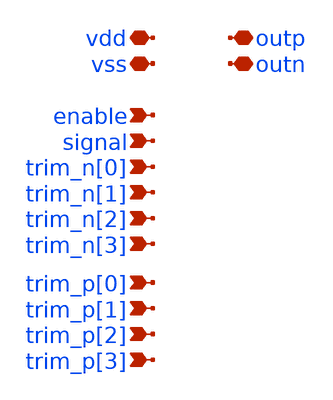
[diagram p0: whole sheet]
** sch_path: xschem/untitled.sch
**.subckt untitled enable signal trim_n[0] trim_n[1] trim_n[2] trim_n[3] trim_p[0] trim_p[1]
*+ trim_p[2] trim_p[3] vss vdd outp outn
*.ipin enable
*.ipin signal
*.ipin trim_n[0]
*.ipin trim_n[1]
*.ipin trim_n[2]
*.ipin trim_n[3]
*.ipin trim_p[0]
*.ipin trim_p[1]
*.ipin trim_p[2]
*.ipin trim_p[3]
*.iopin vss
*.iopin vdd
*.iopin outp
*.iopin outn
**** begin user architecture code


.subckt injector_flat enable outn outp signal trim_n[0] trim_n[1] trim_n[2] trim_n[3]  trim_p[0]
+ trim_p[1] trim_p[2] trim_p[3] vss vdd
X0 vdd a_9644_7080# a_9556_7124# vdd pmos_6p0 w=1.22u l=1u
X1 outn _00_ vss vss nmos_6p0 w=0.82u l=0.6u
X2 vdd _21_ a_2500_4539# vdd pmos_6p0 w=0.62u l=0.5u
X3 _13_ a_8412_4728# vss vss nmos_6p0 w=0.82u l=0.6u
X4 outn _00_ vdd vdd pmos_6p0 w=1.22u l=0.5u
X5 a_2588_5512# a_2500_5556# vss vss nmos_6p0 w=0.82u l=1u
X6 vdd a_3036_5079# a_2948_5176# vdd pmos_6p0 w=1.22u l=1u
X7 a_3044_3229# a_2612_3229# vss vss nmos_6p0 w=0.36u l=0.6u
X8 outp _00_ vdd vdd pmos_6p0 w=1.22u l=0.5u
X9 vdd _08_ outp vdd pmos_6p0 w=1.22u l=0.5u
X10 outn _01_ vdd vdd pmos_6p0 w=1.22u l=0.5u
X11 outn _01_ vss vss nmos_6p0 w=0.82u l=0.6u
X12 outn _00_ vss vss nmos_6p0 w=0.82u l=0.6u
X13 vdd _00_ outp vdd pmos_6p0 w=1.22u l=0.5u
X14 vss a_17700_7124# _07_ vss nmos_6p0 w=0.82u l=0.6u
X15 vdd _24_ a_7092_3229# vdd pmos_6p0 w=0.62u l=0.5u
X16 vss trim_p[1] a_7204_7933# vss nmos_6p0 w=0.36u l=0.6u
X17 outp _00_ vdd vdd pmos_6p0 w=1.22u l=0.5u
X18 outn _00_ vdd vdd pmos_6p0 w=1.22u l=0.5u
X19 _00_ enable vdd vdd pmos_6p0 w=1.22u l=0.5u
X20 outn _00_ vdd vdd pmos_6p0 w=1.22u l=0.5u
X21 outp _00_ vdd vdd pmos_6p0 w=1.22u l=0.5u
X22 a_8573_7889# _00_ vss vss nmos_6p0 w=0.36u l=0.6u
X23 vdd _14_ outp vdd pmos_6p0 w=1.22u l=0.5u
X24 outp _00_ vdd vdd pmos_6p0 w=1.22u l=0.5u
X25 a_16812_3944# a_16724_3988# vss vss nmos_6p0 w=0.82u l=1u
X26 outp _00_ vss vss nmos_6p0 w=0.82u l=0.6u
X27 vdd _00_ outn vdd pmos_6p0 w=1.22u l=0.5u
X28 vdd a_16924_7080# a_16836_7124# vdd pmos_6p0 w=1.22u l=1u
X29 a_15171_7933# a_14708_7933# vss vss nmos_6p0 w=0.36u l=0.6u
X30 vdd a_3484_5079# a_3396_5176# vdd pmos_6p0 w=1.22u l=1u
X31 outn _00_ vdd vdd pmos_6p0 w=1.22u l=0.5u
X32 outp _00_ vss vss nmos_6p0 w=0.82u l=0.6u
X33 vdd _17_ outn vdd pmos_6p0 w=1.22u l=0.5u
X34 a_16280_3604# trim_n[3] vss vss nmos_6p0 w=0.36u l=0.6u
X35 outp _00_ vdd vdd pmos_6p0 w=1.22u l=0.5u
X36 a_12575_3988# a_12132_4539# vdd vdd pmos_6p0 w=0.62u l=0.5u
X37 vdd _26_ a_11124_3229# vdd pmos_6p0 w=0.62u l=0.5u
X38 a_3044_3229# a_2612_3229# a_3004_3696# vdd pmos_6p0 w=0.62u l=0.5u
X39 a_5724_5512# a_5636_5556# vss vss nmos_6p0 w=0.82u l=1u
X40 a_3981_7889# _00_ vss vss nmos_6p0 w=0.36u l=0.6u
X41 outp _00_ vss vss nmos_6p0 w=0.82u l=0.6u
X42 outp _00_ vdd vdd pmos_6p0 w=1.22u l=0.5u
X43 outn _00_ vss vss nmos_6p0 w=0.82u l=0.6u
X44 a_2588_6647# a_2500_6744# vss vss nmos_6p0 w=0.82u l=1u
X45 a_12892_5079# a_12804_5176# vss vss nmos_6p0 w=0.82u l=1u
X46 a_15375_7124# a_14932_7675# vdd vdd pmos_6p0 w=0.62u l=0.5u
X47 _26_ a_5836_3160# vss vss nmos_6p0 w=0.82u l=0.6u
X48 a_16280_3604# trim_n[3] vdd vdd pmos_6p0 w=0.62u l=0.5u
X49 a_1692_5512# a_1604_5556# vss vss nmos_6p0 w=0.82u l=1u
X50 _21_ a_2028_3160# vss vss nmos_6p0 w=0.82u l=0.6u
X51 outn a_7555_4539# vss vss nmos_6p0 w=0.82u l=0.6u
X52 vss _11_ outn vss nmos_6p0 w=0.82u l=0.6u
X53 vdd a_2140_5079# a_2052_5176# vdd pmos_6p0 w=1.22u l=1u
X54 outn _13_ vdd vdd pmos_6p0 w=1.22u l=0.5u
X55 vss a_8328_3604# a_7555_3229# vss nmos_6p0 w=0.36u l=0.6u
X56 a_16851_4797# a_16388_4797# vss vss nmos_6p0 w=0.36u l=0.6u
X57 outp _00_ vdd vdd pmos_6p0 w=1.22u l=0.5u
X58 a_7524_7675# a_7092_7156# vss vss nmos_6p0 w=0.36u l=0.6u
X59 vss a_3044_7675# outp vss nmos_6p0 w=0.82u l=0.6u
X60 a_15487_3728# a_16280_3604# a_15507_3229# vdd pmos_6p0 w=0.62u l=0.5u
X61 vss a_17028_6744# _08_ vss nmos_6p0 w=0.82u l=0.6u
X62 a_12595_4539# a_12132_4539# vss vss nmos_6p0 w=0.36u l=0.6u
X63 _25_ a_6508_3160# vss vss nmos_6p0 w=0.82u l=0.6u
X64 a_6508_6647# a_6420_6744# vss vss nmos_6p0 w=0.82u l=1u
X65 outp _00_ vss vss nmos_6p0 w=0.82u l=0.6u
X66 vss trim_n[0] a_2612_3229# vss nmos_6p0 w=0.36u l=0.6u
X67 vss a_3044_3229# outp vss nmos_6p0 w=0.82u l=0.6u
X68 outn a_2963_4539# vss vss nmos_6p0 w=0.82u l=0.6u
X69 outp a_15151_8432# vdd vdd pmos_6p0 w=1.095u l=0.5u
X70 _02_ a_5636_8000# vss vss nmos_6p0 w=0.82u l=0.6u
X71 vdd a_16700_8215# a_16612_8312# vdd pmos_6p0 w=1.22u l=1u
X72 a_12360_8308# trim_p[2] vss vss nmos_6p0 w=0.36u l=0.6u
X73 a_3036_5512# a_2948_5556# vss vss nmos_6p0 w=0.82u l=1u
X74 _03_ a_4771_7124# vdd vdd pmos_6p0 w=1.22u l=0.5u
X75 vdd a_17932_8215# a_17844_8312# vdd pmos_6p0 w=1.22u l=1u
X76 vdd a_4828_5512# a_4740_5556# vdd pmos_6p0 w=1.22u l=1u
X77 a_3505_6296# _00_ vss vss nmos_6p0 w=0.36u l=0.6u
X78 vdd a_8573_7889# a_7596_8400# vdd pmos_6p0 w=0.62u l=0.5u
X79 vdd a_4492_3944# a_4404_3988# vdd pmos_6p0 w=1.22u l=1u
X80 a_2943_3988# a_3736_3976# a_2963_4539# vdd pmos_6p0 w=0.62u l=0.5u
X81 vss a_3505_6296# _04_ vss nmos_6p0 w=0.82u l=0.6u
X82 vdd a_8461_7553# a_7484_7156# vdd pmos_6p0 w=0.62u l=0.5u
X83 a_4828_4728# a_4828_4728# vdd vdd pmos_6p0 w=1.22u l=0.5u
X84 a_1692_6647# a_1604_6744# vss vss nmos_6p0 w=0.82u l=1u
X85 vss trim_p[2] a_12020_7156# vss nmos_6p0 w=0.36u l=0.6u
X86 vss a_16280_3604# a_15507_3229# vss nmos_6p0 w=0.36u l=0.6u
X87 vss a_3044_7933# outn vss nmos_6p0 w=0.82u l=0.6u
X88 outp _00_ vss vss nmos_6p0 w=0.82u l=0.6u
X89 a_3484_5512# a_3396_5556# vss vss nmos_6p0 w=0.82u l=1u
X90 _01_ a_1716_8000# vss vss nmos_6p0 w=0.82u l=0.6u
X91 vdd a_9644_3944# a_9556_3988# vdd pmos_6p0 w=1.22u l=1u
X92 a_5612_6647# a_5524_6744# vss vss nmos_6p0 w=0.82u l=1u
X93 vdd a_14012_8215# a_13924_8312# vdd pmos_6p0 w=1.22u l=1u
X94 outp _00_ vss vss nmos_6p0 w=0.82u l=0.6u
X95 vdd trim_n[1] a_7535_3988# vdd pmos_6p0 w=0.62u l=0.5u
X96 a_12412_7156# trim_p[2] a_12452_7675# vss nmos_6p0 w=0.36u l=0.6u
X97 vdd _03_ a_5636_8000# vdd pmos_6p0 w=0.565u l=0.5u
X98 a_3036_6647# a_2948_6744# vss vss nmos_6p0 w=0.82u l=1u
X99 a_7555_3229# a_7092_3229# vss vss nmos_6p0 w=0.36u l=0.6u
X100 a_3981_7553# _00_ vdd vdd pmos_6p0 w=0.62u l=0.5u
X101 a_16831_5296# a_17624_5172# a_16851_4797# vdd pmos_6p0 w=0.62u l=0.5u
X102 vdd a_17700_5556# a_17700_5556# vdd pmos_6p0 w=1.22u l=0.5u
X103 vss _03_ a_5636_8000# vss nmos_6p0 w=0.36u l=0.6u
X104 a_2140_5512# a_2052_5556# vss vss nmos_6p0 w=0.82u l=1u
X105 vdd a_3932_5512# a_3844_5556# vdd pmos_6p0 w=1.22u l=1u
X106 a_4771_7124# _00_ vss vss nmos_6p0 w=0.36u l=0.6u
X107 a_3044_7933# a_2612_7933# a_3004_8400# vdd pmos_6p0 w=0.62u l=0.5u
X108 vdd a_2588_6647# a_2500_6744# vdd pmos_6p0 w=1.22u l=1u
X109 a_8573_7889# _00_ vdd vdd pmos_6p0 w=0.62u l=0.5u
X110 a_8461_7553# _00_ vdd vdd pmos_6p0 w=0.62u l=0.5u
X111 a_3004_3696# trim_n[0] vdd vdd pmos_6p0 w=0.62u l=0.5u
X112 vss _15_ outn vss nmos_6p0 w=0.82u l=0.6u
X113 vss a_12360_8308# a_11587_7933# vss nmos_6p0 w=0.36u l=0.6u
X114 a_3004_3696# trim_n[0] a_3044_3229# vss nmos_6p0 w=0.36u l=0.6u
X115 a_15151_8432# a_14708_7933# vdd vdd pmos_6p0 w=0.62u l=0.5u
X116 vss a_3981_7889# a_3044_7933# vss nmos_6p0 w=0.36u l=0.6u
X117 _20_ a_16364_4428# vss vss nmos_6p0 w=0.82u l=0.6u
X118 outn a_12595_4539# vss vss nmos_6p0 w=0.82u l=0.6u
X119 a_11587_3229# a_11124_3229# vss vss nmos_6p0 w=0.36u l=0.6u
X120 vdd a_2588_5512# a_2500_5556# vdd pmos_6p0 w=1.22u l=1u
X121 vdd a_17028_6744# a_17028_6744# vdd pmos_6p0 w=1.22u l=0.5u
X122 a_5836_4428# a_5836_4428# vdd vdd pmos_6p0 w=1.22u l=0.5u
X123 vdd a_6508_6647# a_6420_6744# vdd pmos_6p0 w=1.22u l=1u
X124 a_3981_7889# _00_ vdd vdd pmos_6p0 w=0.62u l=0.5u
X125 outn _09_ vdd vdd pmos_6p0 w=1.22u l=0.5u
X126 outp _02_ vdd vdd pmos_6p0 w=1.22u l=0.5u
X127 a_15507_3229# trim_n[3] a_15487_3728# vss nmos_6p0 w=0.36u l=0.6u
X128 a_5276_5512# a_5188_5556# vss vss nmos_6p0 w=0.82u l=1u
X129 vss a_3736_3976# a_2963_4539# vss nmos_6p0 w=0.36u l=0.6u
X130 vdd a_7484_7156# outp vdd pmos_6p0 w=1.095u l=0.5u
X131 vdd trim_n[1] a_7535_3728# vdd pmos_6p0 w=0.62u l=0.5u
X132 vdd trim_p[3] a_15375_7124# vdd pmos_6p0 w=0.62u l=0.5u
X133 a_16364_6296# a_16364_6296# vdd vdd pmos_6p0 w=1.22u l=0.5u
X134 vdd a_7596_8400# outn vdd pmos_6p0 w=1.095u l=0.5u
X135 outn _00_ vdd vdd pmos_6p0 w=1.22u l=0.5u
X136 outn _00_ vss vss nmos_6p0 w=0.82u l=0.6u
X137 vdd a_12892_5079# a_12804_5176# vdd pmos_6p0 w=1.22u l=1u
X138 vdd a_16812_3944# a_16724_3988# vdd pmos_6p0 w=1.22u l=1u
X139 vdd _11_ outn vdd pmos_6p0 w=1.22u l=0.5u
X140 a_16831_5296# a_16388_4797# vdd vdd pmos_6p0 w=0.62u l=0.5u
X141 outn _00_ vss vss nmos_6p0 w=0.82u l=0.6u
X142 a_2140_6647# a_2052_6744# vss vss nmos_6p0 w=0.82u l=1u
X143 outn _00_ vdd vdd pmos_6p0 w=1.22u l=0.5u
X144 outp _00_ vdd vdd pmos_6p0 w=1.22u l=0.5u
X145 outp _00_ vss vss nmos_6p0 w=0.82u l=0.6u
X146 vdd _00_ a_14708_7933# vdd pmos_6p0 w=0.62u l=0.5u
X147 a_12452_7675# a_12020_7156# vss vss nmos_6p0 w=0.36u l=0.6u
X148 vdd trim_n[2] a_11567_3728# vdd pmos_6p0 w=0.62u l=0.5u
X149 vdd a_5724_5512# a_5636_5556# vdd pmos_6p0 w=1.22u l=1u
X150 vdd a_1692_6647# a_1604_6744# vdd pmos_6p0 w=1.22u l=1u
X151 outn _00_ vdd vdd pmos_6p0 w=1.22u l=0.5u
X152 a_15395_7675# a_14932_7675# vss vss nmos_6p0 w=0.36u l=0.6u
X153 vdd a_1692_5512# a_1604_5556# vdd pmos_6p0 w=1.22u l=1u
X154 vdd _28_ a_15044_3229# vdd pmos_6p0 w=0.62u l=0.5u
X155 outp _00_ vdd vdd pmos_6p0 w=1.22u l=0.5u
X156 vdd a_5612_6647# a_5524_6744# vdd pmos_6p0 w=1.22u l=1u
X157 a_11587_7933# trim_p[2] a_11567_8432# vss nmos_6p0 w=0.36u l=0.6u
X158 a_9644_5512# a_9556_5556# vss vss nmos_6p0 w=0.82u l=1u
X159 vss _27_ a_16388_4797# vss nmos_6p0 w=0.36u l=0.6u
X160 a_4380_5512# a_4292_5556# vss vss nmos_6p0 w=0.82u l=1u
X161 outn _00_ vss vss nmos_6p0 w=0.82u l=0.6u
X162 vdd trim_n[2] a_12575_3988# vdd pmos_6p0 w=0.62u l=0.5u
X163 a_7535_3728# a_7092_3229# vdd vdd pmos_6p0 w=0.62u l=0.5u
X164 vdd a_3036_6647# a_2948_6744# vdd pmos_6p0 w=1.22u l=1u
X165 a_3044_7933# a_2612_7933# vss vss nmos_6p0 w=0.36u l=0.6u
X166 outp _10_ vdd vdd pmos_6p0 w=1.22u l=0.5u
X167 vss _07_ outn vss nmos_6p0 w=0.82u l=0.6u
X168 outn _00_ vss vss nmos_6p0 w=0.82u l=0.6u
X169 vss _25_ a_12132_4539# vss nmos_6p0 w=0.36u l=0.6u
X170 outn _09_ vss vss nmos_6p0 w=0.82u l=0.6u
X171 outp _02_ vss vss nmos_6p0 w=0.82u l=0.6u
X172 a_2963_4539# trim_n[0] a_2943_3988# vss nmos_6p0 w=0.36u l=0.6u
X173 vdd trim_p[0] a_2612_7156# vdd pmos_6p0 w=0.62u l=0.5u
X174 vss _02_ outn vss nmos_6p0 w=0.82u l=0.6u
X175 outn _00_ vss vss nmos_6p0 w=0.82u l=0.6u
X176 _00_ enable vss vss nmos_6p0 w=0.82u l=0.6u
X177 vss signal_n a_3505_6296# vss nmos_6p0 w=0.36u l=0.6u
X178 outn _00_ vss vss nmos_6p0 w=0.82u l=0.6u
X179 vdd a_3036_5512# a_2948_5556# vdd pmos_6p0 w=1.22u l=1u
X180 vss a_7060_5176# _15_ vss nmos_6p0 w=0.82u l=0.6u
X181 a_4959_7124# _00_ a_4771_7124# vdd pmos_6p0 w=0.565u l=0.5u
X182 a_6396_7080# a_6308_7124# vss vss nmos_6p0 w=0.82u l=1u
X183 a_3004_8400# trim_p[0] vdd vdd pmos_6p0 w=0.62u l=0.5u
X184 a_11567_3728# a_11124_3229# vdd vdd pmos_6p0 w=0.62u l=0.5u
X185 outp _00_ vdd vdd pmos_6p0 w=1.22u l=0.5u
X186 outn _00_ vss vss nmos_6p0 w=0.82u l=0.6u
X187 a_9644_7080# a_9556_7124# vss vss nmos_6p0 w=0.82u l=1u
X188 outp _16_ vss vss nmos_6p0 w=0.82u l=0.6u
X189 outp _00_ vss vss nmos_6p0 w=0.82u l=0.6u
X190 _05_ a_8412_6296# vss vss nmos_6p0 w=0.82u l=0.6u
X191 a_15944_8308# trim_p[3] vdd vdd pmos_6p0 w=0.62u l=0.5u
X192 outn _00_ vdd vdd pmos_6p0 w=1.22u l=0.5u
X193 vss a_15944_8308# a_15171_7933# vss nmos_6p0 w=0.36u l=0.6u
X194 outp _00_ vss vss nmos_6p0 w=0.82u l=0.6u
X195 outp _00_ vss vss nmos_6p0 w=0.82u l=0.6u
X196 vdd a_3484_5512# a_3396_5556# vdd pmos_6p0 w=1.22u l=1u
X197 outp _12_ vss vss nmos_6p0 w=0.82u l=0.6u
X198 a_12412_7156# trim_p[2] vdd vdd pmos_6p0 w=0.62u l=0.5u
X199 a_15171_7933# trim_p[3] a_15151_8432# vss nmos_6p0 w=0.36u l=0.6u
X200 signal_n signal vdd vdd pmos_6p0 w=1.22u l=0.5u
X201 outn _00_ vdd vdd pmos_6p0 w=1.22u l=0.5u
X202 a_16812_5512# a_16724_5556# vss vss nmos_6p0 w=0.82u l=1u
X203 outp _00_ vss vss nmos_6p0 w=0.82u l=0.6u
X204 vdd a_2140_6647# a_2052_6744# vdd pmos_6p0 w=1.22u l=1u
X205 a_16924_7080# a_16836_7124# vss vss nmos_6p0 w=0.82u l=1u
X206 outp _00_ vss vss nmos_6p0 w=0.82u l=0.6u
X207 a_13389_7553# _00_ vdd vdd pmos_6p0 w=0.62u l=0.5u
X208 a_3981_7553# _00_ vss vss nmos_6p0 w=0.36u l=0.6u
X209 a_7636_7933# a_7204_7933# a_7596_8400# vdd pmos_6p0 w=0.62u l=0.5u
X210 a_7535_3988# a_8328_3976# a_7555_4539# vdd pmos_6p0 w=0.62u l=0.5u
X211 outp _00_ vss vss nmos_6p0 w=0.82u l=0.6u
X212 vss _23_ a_7092_4539# vss nmos_6p0 w=0.36u l=0.6u
X213 vss trim_p[1] a_7092_7156# vss nmos_6p0 w=0.36u l=0.6u
X214 outp _10_ vss vss nmos_6p0 w=0.82u l=0.6u
X215 vdd trim_p[1] a_7204_7933# vdd pmos_6p0 w=0.62u l=0.5u
X216 vdd _00_ a_11124_7933# vdd pmos_6p0 w=0.62u l=0.5u
X217 outn _00_ vdd vdd pmos_6p0 w=1.22u l=0.5u
X218 a_8461_7553# _00_ vss vss nmos_6p0 w=0.36u l=0.6u
X219 a_8328_3976# trim_n[1] vss vss nmos_6p0 w=0.36u l=0.6u
X220 vdd a_2140_5512# a_2052_5556# vdd pmos_6p0 w=1.22u l=1u
X221 vss trim_p[0] a_2612_7933# vss nmos_6p0 w=0.36u l=0.6u
X222 a_7484_7156# trim_p[1] vdd vdd pmos_6p0 w=0.62u l=0.5u
X223 vdd trim_p[2] a_11567_8432# vdd pmos_6p0 w=0.62u l=0.5u
X224 vss a_7636_7933# outn vss nmos_6p0 w=0.82u l=0.6u
X225 outp _00_ vss vss nmos_6p0 w=0.82u l=0.6u
X226 vdd signal a_4959_7124# vdd pmos_6p0 w=0.565u l=0.5u
X227 a_10204_4428# a_10204_4428# vdd vdd pmos_6p0 w=1.22u l=0.5u
X228 outp _00_ vss vss nmos_6p0 w=0.82u l=0.6u
X229 vdd _15_ outn vdd pmos_6p0 w=1.22u l=0.5u
X230 a_12892_6647# a_12804_6744# vss vss nmos_6p0 w=0.82u l=1u
X231 vss a_6836_5556# _17_ vss nmos_6p0 w=0.82u l=0.6u
X232 outn _05_ vdd vdd pmos_6p0 w=1.22u l=0.5u
X233 a_3736_3976# trim_n[0] vss vss nmos_6p0 w=0.36u l=0.6u
X234 vss _26_ a_11124_3229# vss nmos_6p0 w=0.36u l=0.6u
X235 a_4828_3160# a_4828_3160# vdd vdd pmos_6p0 w=1.22u l=0.5u
X236 outn _00_ vdd vdd pmos_6p0 w=1.22u l=0.5u
X237 outn _00_ vss vss nmos_6p0 w=0.82u l=0.6u
X238 vdd a_5276_5512# a_5188_5556# vdd pmos_6p0 w=1.22u l=1u
X239 a_7535_3728# a_8328_3604# a_7555_3229# vdd pmos_6p0 w=0.62u l=0.5u
X240 vdd a_3981_3185# a_3004_3696# vdd pmos_6p0 w=0.62u l=0.5u
X241 a_15375_7124# a_16168_7112# a_15395_7675# vdd pmos_6p0 w=0.62u l=0.5u
X242 a_4044_4728# a_4044_4728# vdd vdd pmos_6p0 w=1.22u l=0.5u
X243 a_15507_3229# a_15044_3229# vss vss nmos_6p0 w=0.36u l=0.6u
X244 _03_ a_4771_7124# vss vss nmos_6p0 w=0.82u l=0.6u
X245 outp a_7535_3728# vdd vdd pmos_6p0 w=1.095u l=0.5u
X246 vdd _06_ outp vdd pmos_6p0 w=1.22u l=0.5u
X247 vss a_8573_7889# a_7636_7933# vss nmos_6p0 w=0.36u l=0.6u
X248 _28_ a_4828_4728# vss vss nmos_6p0 w=0.82u l=0.6u
X249 a_3505_6296# signal_n a_3897_6875# vdd pmos_6p0 w=0.565u l=0.5u
X250 outn _00_ vdd vdd pmos_6p0 w=1.22u l=0.5u
X251 vdd _23_ a_7092_4539# vdd pmos_6p0 w=0.62u l=0.5u
X252 vdd _07_ outn vdd pmos_6p0 w=1.22u l=0.5u
X253 outn _00_ vss vss nmos_6p0 w=0.82u l=0.6u
X254 outp a_7555_3229# vss vss nmos_6p0 w=0.82u l=0.6u
X255 outn a_16831_5296# vdd vdd pmos_6p0 w=1.095u l=0.5u
X256 a_15944_8308# trim_p[3] vss vss nmos_6p0 w=0.36u l=0.6u
X257 a_5164_4428# a_5164_4428# vdd vdd pmos_6p0 w=1.22u l=0.5u
X258 a_6060_6647# a_5972_6744# vss vss nmos_6p0 w=0.82u l=1u
X259 vss a_15684_3988# _14_ vss nmos_6p0 w=0.82u l=0.6u
X260 outp a_11567_3728# vdd vdd pmos_6p0 w=1.095u l=0.5u
X261 a_14684_3511# a_14596_3608# vss vss nmos_6p0 w=0.82u l=1u
X262 a_7740_4728# a_7740_4728# vdd vdd pmos_6p0 w=1.22u l=0.5u
X263 vss _00_ a_14932_7675# vss nmos_6p0 w=0.36u l=0.6u
X264 a_12595_4539# trim_n[2] a_12575_3988# vss nmos_6p0 w=0.36u l=0.6u
X265 a_17932_3511# a_17844_3608# vss vss nmos_6p0 w=0.82u l=1u
X266 vdd a_7060_5176# a_7060_5176# vdd pmos_6p0 w=1.22u l=0.5u
X267 vdd trim_n[3] a_15487_3728# vdd pmos_6p0 w=0.62u l=0.5u
X268 a_3004_8400# trim_p[0] a_3044_7933# vss nmos_6p0 w=0.36u l=0.6u
X269 vdd a_9644_5512# a_9556_5556# vdd pmos_6p0 w=1.22u l=1u
X270 a_2943_3988# a_2500_4539# vdd vdd pmos_6p0 w=0.62u l=0.5u
X271 a_8412_4728# a_8412_4728# vdd vdd pmos_6p0 w=1.22u l=0.5u
X272 _23_ a_5836_4428# vss vss nmos_6p0 w=0.82u l=0.6u
X273 vdd a_4380_5512# a_4292_5556# vdd pmos_6p0 w=1.22u l=1u
X274 a_11587_7933# a_11124_7933# vss vss nmos_6p0 w=0.36u l=0.6u
X275 outp _20_ vdd vdd pmos_6p0 w=1.22u l=0.5u
X276 outp a_11587_3229# vss vss nmos_6p0 w=0.82u l=0.6u
X277 outp a_15487_3728# vdd vdd pmos_6p0 w=1.095u l=0.5u
X278 a_12575_3988# a_13368_3976# a_12595_4539# vdd pmos_6p0 w=0.62u l=0.5u
X279 outn _00_ vdd vdd pmos_6p0 w=1.22u l=0.5u
X280 vdd a_17700_7124# a_17700_7124# vdd pmos_6p0 w=1.22u l=0.5u
X281 vss a_3981_7553# a_3044_7675# vss nmos_6p0 w=0.36u l=0.6u
X282 outp _00_ vss vss nmos_6p0 w=0.82u l=0.6u
X283 _02_ a_5636_8000# vdd vdd pmos_6p0 w=1.22u l=0.5u
X284 a_16700_8215# a_16612_8312# vss vss nmos_6p0 w=0.82u l=1u
X285 a_13368_3976# trim_n[2] vss vss nmos_6p0 w=0.36u l=0.6u
X286 vss _18_ outp vss nmos_6p0 w=0.82u l=0.6u
X287 a_5836_3160# a_5836_3160# vdd vdd pmos_6p0 w=1.22u l=0.5u
X288 vdd a_12892_6647# a_12804_6744# vdd pmos_6p0 w=1.22u l=1u
X289 vss a_15012_3988# _06_ vss nmos_6p0 w=0.82u l=0.6u
X290 a_17932_8215# a_17844_8312# vss vss nmos_6p0 w=0.82u l=1u
X291 a_2028_3160# a_2028_3160# vdd vdd pmos_6p0 w=1.22u l=0.5u
X292 a_2963_4539# a_2500_4539# vss vss nmos_6p0 w=0.36u l=0.6u
X293 outp _00_ vdd vdd pmos_6p0 w=1.22u l=0.5u
X294 outn _00_ vdd vdd pmos_6p0 w=1.22u l=0.5u
X295 outn _00_ vss vss nmos_6p0 w=0.82u l=0.6u
X296 outn _00_ vdd vdd pmos_6p0 w=1.22u l=0.5u
X297 outp _00_ vdd vdd pmos_6p0 w=1.22u l=0.5u
X298 vdd trim_p[3] a_15151_8432# vdd pmos_6p0 w=0.62u l=0.5u
X299 outp a_11587_7933# vss vss nmos_6p0 w=0.82u l=0.6u
X300 a_6508_3160# a_6508_3160# vdd vdd pmos_6p0 w=1.22u l=0.5u
X301 a_7636_7933# a_7204_7933# vss vss nmos_6p0 w=0.36u l=0.6u
X302 vss a_9860_3608# _11_ vss nmos_6p0 w=0.82u l=0.6u
X303 vss a_12452_7675# outn vss nmos_6p0 w=0.82u l=0.6u
X304 a_2588_5079# a_2500_5176# vss vss nmos_6p0 w=0.82u l=1u
X305 a_7555_4539# trim_n[1] a_7535_3988# vss nmos_6p0 w=0.36u l=0.6u
X306 vss _01_ outp vss nmos_6p0 w=0.82u l=0.6u
X307 a_15487_3728# a_15044_3229# vdd vdd pmos_6p0 w=0.62u l=0.5u
X308 outp _00_ vdd vdd pmos_6p0 w=1.22u l=0.5u
X309 _16_ a_9084_6296# vss vss nmos_6p0 w=0.82u l=0.6u
X310 outn _00_ vdd vdd pmos_6p0 w=1.22u l=0.5u
X311 a_13389_7553# _00_ vss vss nmos_6p0 w=0.36u l=0.6u
X312 _01_ a_1716_8000# vdd vdd pmos_6p0 w=1.22u l=0.5u
X313 outp a_11567_8432# vdd vdd pmos_6p0 w=1.095u l=0.5u
X314 outn a_12575_3988# vdd vdd pmos_6p0 w=1.095u l=0.5u
X315 vdd trim_p[2] a_12020_7156# vdd pmos_6p0 w=0.62u l=0.5u
X316 outp _00_ vss vss nmos_6p0 w=0.82u l=0.6u
X317 a_8328_3976# trim_n[1] vdd vdd pmos_6p0 w=0.62u l=0.5u
X318 vdd a_16812_5512# a_16724_5556# vdd pmos_6p0 w=1.22u l=1u
X319 a_3044_7675# a_2612_7156# a_3004_7156# vdd pmos_6p0 w=0.62u l=0.5u
X320 a_14012_8215# a_13924_8312# vss vss nmos_6p0 w=0.82u l=1u
X321 outn _00_ vss vss nmos_6p0 w=0.82u l=0.6u
X322 vdd a_3505_6296# _04_ vdd pmos_6p0 w=1.22u l=0.5u
X323 outn a_15375_7124# vdd vdd pmos_6p0 w=1.095u l=0.5u
X324 vdd trim_n[3] a_16831_5296# vdd pmos_6p0 w=0.62u l=0.5u
X325 vss a_7524_7675# outp vss nmos_6p0 w=0.82u l=0.6u
X326 vss signal a_4771_7124# vss nmos_6p0 w=0.36u l=0.6u
X327 a_3981_3185# _22_ vss vss nmos_6p0 w=0.36u l=0.6u
X328 vss a_17624_5172# a_16851_4797# vss nmos_6p0 w=0.36u l=0.6u
X329 a_3897_6875# _00_ vdd vdd pmos_6p0 w=0.565u l=0.5u
X330 vdd _25_ a_12132_4539# vdd pmos_6p0 w=0.62u l=0.5u
X331 _12_ a_16364_6296# vss vss nmos_6p0 w=0.82u l=0.6u
X332 a_3736_3976# trim_n[0] vdd vdd pmos_6p0 w=0.62u l=0.5u
X333 vdd a_6060_6647# a_5972_6744# vdd pmos_6p0 w=1.22u l=1u
X334 vss _24_ a_7092_3229# vss nmos_6p0 w=0.36u l=0.6u
X335 vdd a_14684_3511# a_14596_3608# vdd pmos_6p0 w=1.22u l=1u
X336 vss a_13368_3976# a_12595_4539# vss nmos_6p0 w=0.36u l=0.6u
X337 vdd a_17932_3511# a_17844_3608# vdd pmos_6p0 w=1.22u l=1u
X338 vss a_7732_6744# _19_ vss nmos_6p0 w=0.82u l=0.6u
X339 a_8328_3604# trim_n[1] vss vss nmos_6p0 w=0.36u l=0.6u
X340 vdd a_6836_5556# a_6836_5556# vdd pmos_6p0 w=1.22u l=0.5u
X341 a_3044_7675# a_2612_7156# vss vss nmos_6p0 w=0.36u l=0.6u
X342 vdd trim_n[0] a_2612_3229# vdd pmos_6p0 w=0.62u l=0.5u
X343 vdd _00_ a_14932_7675# vdd pmos_6p0 w=0.62u l=0.5u
X344 outp _00_ vdd vdd pmos_6p0 w=1.22u l=0.5u
X345 a_1692_5079# a_1604_5176# vss vss nmos_6p0 w=0.82u l=1u
X346 vss _08_ outp vss nmos_6p0 w=0.82u l=0.6u
X347 outn _00_ vss vss nmos_6p0 w=0.82u l=0.6u
X348 outn _00_ vss vss nmos_6p0 w=0.82u l=0.6u
X349 a_8328_3604# trim_n[1] vdd vdd pmos_6p0 w=0.62u l=0.5u
X350 a_16168_7112# trim_p[3] vdd vdd pmos_6p0 w=0.62u l=0.5u
X351 a_12360_3604# trim_n[2] vss vss nmos_6p0 w=0.36u l=0.6u
X352 outn a_7535_3988# vdd vdd pmos_6p0 w=1.095u l=0.5u
X353 outn a_16851_4797# vss vss nmos_6p0 w=0.82u l=0.6u
X354 vss _14_ outp vss nmos_6p0 w=0.82u l=0.6u
X355 outn _00_ vss vss nmos_6p0 w=0.82u l=0.6u
X356 outn _13_ vss vss nmos_6p0 w=0.82u l=0.6u
X357 vss _19_ outn vss nmos_6p0 w=0.82u l=0.6u
X358 vss _28_ a_15044_3229# vss nmos_6p0 w=0.36u l=0.6u
X359 vss signal signal_n vss nmos_6p0 w=0.82u l=0.6u
X360 a_17624_5172# trim_n[3] vdd vdd pmos_6p0 w=0.62u l=0.5u
X361 outp _00_ vss vss nmos_6p0 w=0.82u l=0.6u
X362 vdd signal signal_n vdd pmos_6p0 w=1.22u l=0.5u
X363 a_15395_7675# trim_p[3] a_15375_7124# vss nmos_6p0 w=0.36u l=0.6u
X364 a_11567_8432# a_11124_7933# vdd vdd pmos_6p0 w=0.62u l=0.5u
X365 vss _17_ outn vss nmos_6p0 w=0.82u l=0.6u
X366 a_12360_3604# trim_n[2] vdd vdd pmos_6p0 w=0.62u l=0.5u
X367 a_3036_5079# a_2948_5176# vss vss nmos_6p0 w=0.82u l=1u
X368 outn a_2943_3988# vdd vdd pmos_6p0 w=1.095u l=0.5u
X369 a_7596_8400# trim_p[1] a_7636_7933# vss nmos_6p0 w=0.36u l=0.6u
X370 vdd a_9860_3608# a_9860_3608# vdd pmos_6p0 w=1.22u l=0.5u
X371 a_11567_3728# a_12360_3604# a_11587_3229# vdd pmos_6p0 w=0.62u l=0.5u
X372 a_16851_4797# trim_n[3] a_16831_5296# vss nmos_6p0 w=0.36u l=0.6u
X373 vdd a_15684_3988# a_15684_3988# vdd pmos_6p0 w=1.22u l=0.5u
X374 vss a_8328_3976# a_7555_4539# vss nmos_6p0 w=0.36u l=0.6u
X375 vdd _01_ outp vdd pmos_6p0 w=1.22u l=0.5u
X376 a_15151_8432# a_15944_8308# a_15171_7933# vdd pmos_6p0 w=0.62u l=0.5u
X377 _10_ a_10204_4428# vss vss nmos_6p0 w=0.82u l=0.6u
X378 outp _00_ vdd vdd pmos_6p0 w=1.22u l=0.5u
X379 vdd _18_ outp vdd pmos_6p0 w=1.22u l=0.5u
X380 signal_n signal vss vss nmos_6p0 w=0.82u l=0.6u
X381 a_16168_7112# trim_p[3] vss vss nmos_6p0 w=0.36u l=0.6u
X382 outp a_15171_7933# vss vss nmos_6p0 w=0.82u l=0.6u
X383 outn _05_ vss vss nmos_6p0 w=0.82u l=0.6u
X384 a_3484_5079# a_3396_5176# vss vss nmos_6p0 w=0.82u l=1u
X385 vss trim_p[0] a_2612_7156# vss nmos_6p0 w=0.36u l=0.6u
X386 a_13368_3976# trim_n[2] vdd vdd pmos_6p0 w=0.62u l=0.5u
X387 vdd a_13389_7553# a_12412_7156# vdd pmos_6p0 w=0.62u l=0.5u
X388 outp _00_ vdd vdd pmos_6p0 w=1.22u l=0.5u
X389 a_3981_3185# _22_ vdd vdd pmos_6p0 w=0.62u l=0.5u
X390 a_3004_7156# trim_p[0] vdd vdd pmos_6p0 w=0.62u l=0.5u
X391 vss _00_ outp vss nmos_6p0 w=0.82u l=0.6u
X392 vss _00_ a_11124_7933# vss nmos_6p0 w=0.36u l=0.6u
X393 vdd a_3004_3696# outp vdd pmos_6p0 w=1.095u l=0.5u
X394 vdd _02_ outn vdd pmos_6p0 w=1.22u l=0.5u
X395 vdd a_2588_5079# a_2500_5176# vdd pmos_6p0 w=1.22u l=1u
X396 vdd a_3981_7553# a_3004_7156# vdd pmos_6p0 w=0.62u l=0.5u
X397 vss a_12360_3604# a_11587_3229# vss nmos_6p0 w=0.36u l=0.6u
X398 outp a_15507_3229# vss vss nmos_6p0 w=0.82u l=0.6u
X399 a_4828_5512# a_4740_5556# vss vss nmos_6p0 w=0.82u l=1u
X400 vdd a_7732_6744# a_7732_6744# vdd pmos_6p0 w=1.22u l=0.5u
X401 vdd a_12412_7156# outn vdd pmos_6p0 w=1.095u l=0.5u
X402 vss _00_ outn vss nmos_6p0 w=0.82u l=0.6u
X403 a_2140_5079# a_2052_5176# vss vss nmos_6p0 w=0.82u l=1u
X404 vdd a_15012_3988# a_15012_3988# vdd pmos_6p0 w=1.22u l=0.5u
X405 vss a_3981_3185# a_3044_3229# vss nmos_6p0 w=0.36u l=0.6u
X406 a_4492_3944# a_4404_3988# vss vss nmos_6p0 w=0.82u l=1u
X407 vss _21_ a_2500_4539# vss nmos_6p0 w=0.36u l=0.6u
X408 a_16364_4428# a_16364_4428# vdd vdd pmos_6p0 w=1.22u l=0.5u
X409 vdd trim_n[0] a_2943_3988# vdd pmos_6p0 w=0.62u l=0.5u
X410 a_7535_3988# a_7092_4539# vdd vdd pmos_6p0 w=0.62u l=0.5u
X411 vdd trim_p[0] a_2612_7933# vdd pmos_6p0 w=0.62u l=0.5u
X412 vdd a_3004_7156# outp vdd pmos_6p0 w=1.095u l=0.5u
X413 outn _00_ vdd vdd pmos_6p0 w=1.22u l=0.5u
X414 _27_ a_5164_4428# vss vss nmos_6p0 w=0.82u l=0.6u
X415 outn a_15395_7675# vss vss nmos_6p0 w=0.82u l=0.6u
X416 vdd _04_ a_1716_8000# vdd pmos_6p0 w=0.565u l=0.5u
X417 a_12452_7675# a_12020_7156# a_12412_7156# vdd pmos_6p0 w=0.62u l=0.5u
X418 _22_ a_4044_4728# vss vss nmos_6p0 w=0.82u l=0.6u
X419 vdd a_3981_7889# a_3004_8400# vdd pmos_6p0 w=0.62u l=0.5u
X420 vss a_13389_7553# a_12452_7675# vss nmos_6p0 w=0.36u l=0.6u
X421 vss _04_ a_1716_8000# vss nmos_6p0 w=0.36u l=0.6u
X422 a_9644_3944# a_9556_3988# vss vss nmos_6p0 w=0.82u l=1u
X423 a_7555_3229# trim_n[1] a_7535_3728# vss nmos_6p0 w=0.36u l=0.6u
X424 vdd _19_ outn vdd pmos_6p0 w=1.22u l=0.5u
X425 a_7555_4539# a_7092_4539# vss vss nmos_6p0 w=0.36u l=0.6u
X426 vdd _27_ a_16388_4797# vdd pmos_6p0 w=0.62u l=0.5u
X427 vss a_16168_7112# a_15395_7675# vss nmos_6p0 w=0.36u l=0.6u
X428 vss _06_ outp vss nmos_6p0 w=0.82u l=0.6u
X429 a_7596_8400# trim_p[1] vdd vdd pmos_6p0 w=0.62u l=0.5u
X430 outp _20_ vss vss nmos_6p0 w=0.82u l=0.6u
X431 outp _16_ vdd vdd pmos_6p0 w=1.22u l=0.5u
X432 a_17624_5172# trim_n[3] vss vss nmos_6p0 w=0.36u l=0.6u
X433 vdd a_1692_5079# a_1604_5176# vdd pmos_6p0 w=1.22u l=1u
X434 a_8412_6296# a_8412_6296# vdd vdd pmos_6p0 w=1.22u l=0.5u
X435 outn _00_ vss vss nmos_6p0 w=0.82u l=0.6u
X436 vss _00_ a_14708_7933# vss nmos_6p0 w=0.36u l=0.6u
X437 outn _00_ vdd vdd pmos_6p0 w=1.22u l=0.5u
X438 a_7524_7675# a_7092_7156# a_7484_7156# vdd pmos_6p0 w=0.62u l=0.5u
X439 _24_ a_4828_3160# vss vss nmos_6p0 w=0.82u l=0.6u
X440 vss a_17700_5556# _18_ vss nmos_6p0 w=0.82u l=0.6u
X441 a_12360_8308# trim_p[2] vdd vdd pmos_6p0 w=0.62u l=0.5u
X442 a_3932_5512# a_3844_5556# vss vss nmos_6p0 w=0.82u l=1u
X443 outp _00_ vdd vdd pmos_6p0 w=1.22u l=0.5u
X444 a_3004_7156# trim_p[0] a_3044_7675# vss nmos_6p0 w=0.36u l=0.6u
X445 vdd a_3004_8400# outn vdd pmos_6p0 w=1.095u l=0.5u
X446 _09_ a_7740_4728# vss vss nmos_6p0 w=0.82u l=0.6u
X447 vss a_8461_7553# a_7524_7675# vss nmos_6p0 w=0.36u l=0.6u
X448 a_9084_6296# a_9084_6296# vdd vdd pmos_6p0 w=1.22u l=0.5u
X449 vdd trim_p[1] a_7092_7156# vdd pmos_6p0 w=0.62u l=0.5u
X450 a_11567_8432# a_12360_8308# a_11587_7933# vdd pmos_6p0 w=0.62u l=0.5u
X451 outp _12_ vdd vdd pmos_6p0 w=1.22u l=0.5u
X452 a_11587_3229# trim_n[2] a_11567_3728# vss nmos_6p0 w=0.36u l=0.6u
X453 a_7484_7156# trim_p[1] a_7524_7675# vss nmos_6p0 w=0.36u l=0.6u
X454 vdd a_6396_7080# a_6308_7124# vdd pmos_6p0 w=1.22u l=1u
X455 outp _00_ vdd vdd pmos_6p0 w=1.22u l=0.5u
C0 _25_ _26_ 2.55fF
C1 _18_ _06_ 2.66fF
C2 vdd outn 6.11fF
C3 _00_ outp 9.74fF
C4 _08_ outp 2.26fF
C5 _00_ _08_ 3.52fF
C6 _18_ _00_ 3.43fF
C7 _11_ _28_ 2.29fF
C8 vdd outp 5.92fF
C9 outn outp 2.50fF
C10 vdd _00_ 3.37fF
C11 _00_ outn 6.23fF
C12 _27_ _13_ 4.37fF
C13 trim_n[2] vss 2.73fF
C14 trim_n[1] vss 2.72fF
C15 trim_n[0] vss 2.60fF
C16 trim_n[3] vss 2.99fF
C17 trim_p[3] vss 2.68fF
C18 trim_p[2] vss 2.72fF
C19 trim_p[1] vss 2.65fF
C20 outp vss 7.83fF
C21 outn vss 7.81fF
C22 trim_p[0] vss 2.63fF
C23 vdd vss 178.10fF
C24 _00_ vss 22.17fF $ **FLOATING
.ends



**** end user architecture code
**.ends
.end
